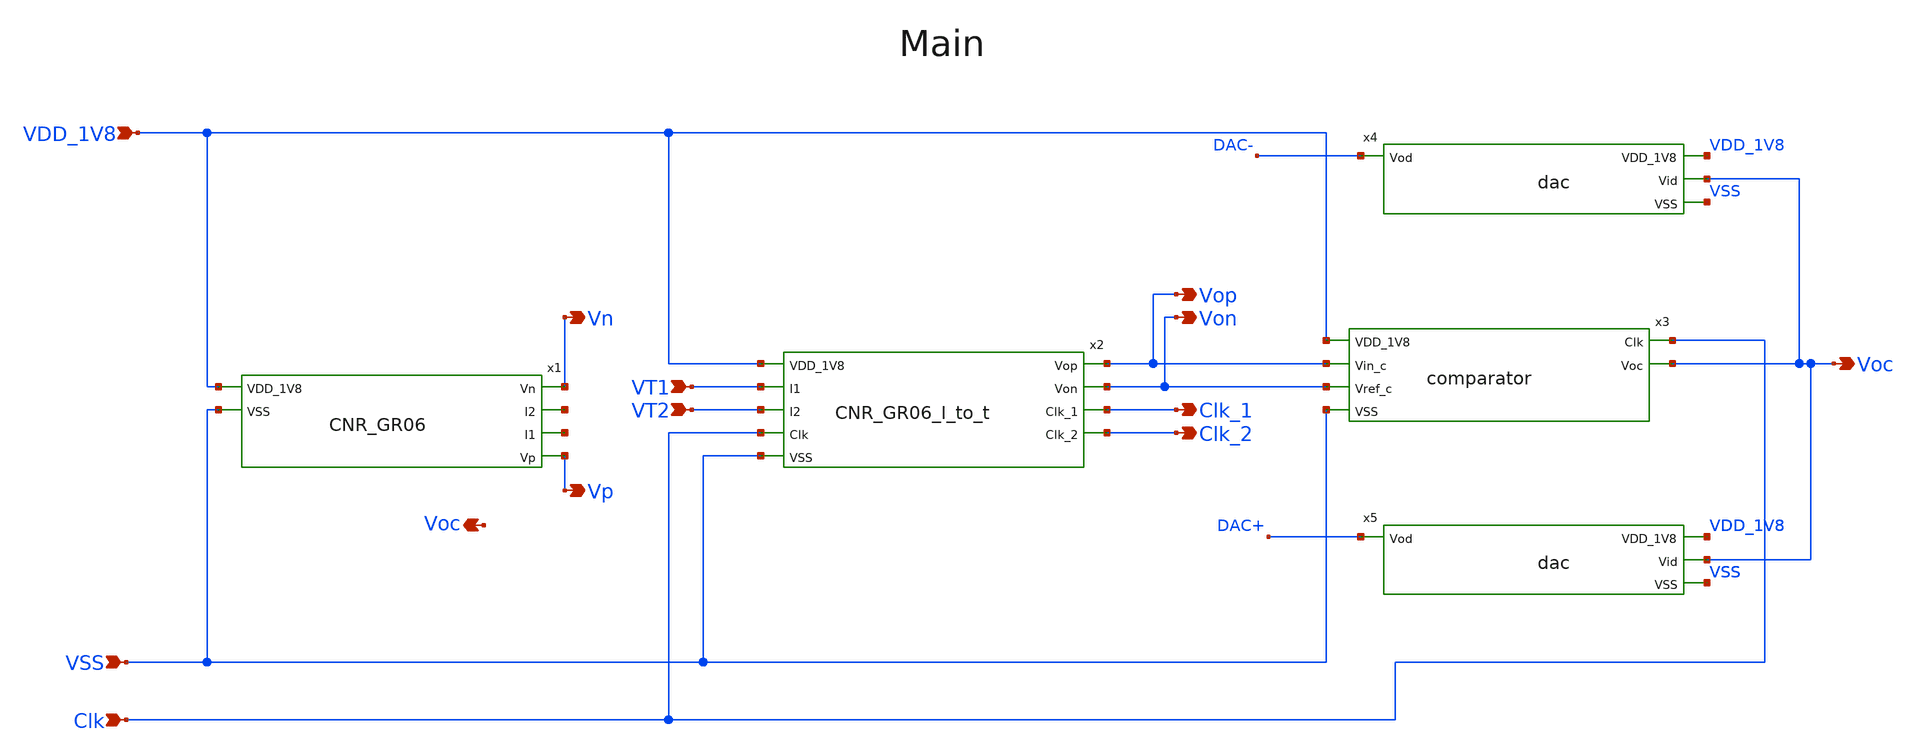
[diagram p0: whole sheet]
** sch_path: design/CNR_GR06_SKY130NM/CNR_GR06_main.sch
**.subckt CNR_GR06_main VDD_1V8 VSS Vn Vp Vop Von Clk_1 Clk_2 Clk VT1 VT2 Voc Voc
*.ipin VDD_1V8
*.ipin VSS
*.opin Vn
*.opin Vp
*.opin Vop
*.opin Von
*.opin Clk_1
*.opin Clk_2
*.ipin Clk
*.ipin VT1
*.ipin VT2
*.opin Voc
*.opin Voc
x1 VDD_1V8 Vn net1 net2 Vp VSS CNR_GR06
x2 VDD_1V8 VT1 Vop Von VT2 Clk_1 Clk Clk_2 VSS CNR_GR06_I_to_t
x3 VDD_1V8 Vop Von Clk Voc VSS comparator
x4 VDD_1V8 Voc DAC- VSS dac
x5 VDD_1V8 Voc DAC+ VSS dac
**.ends
.end
